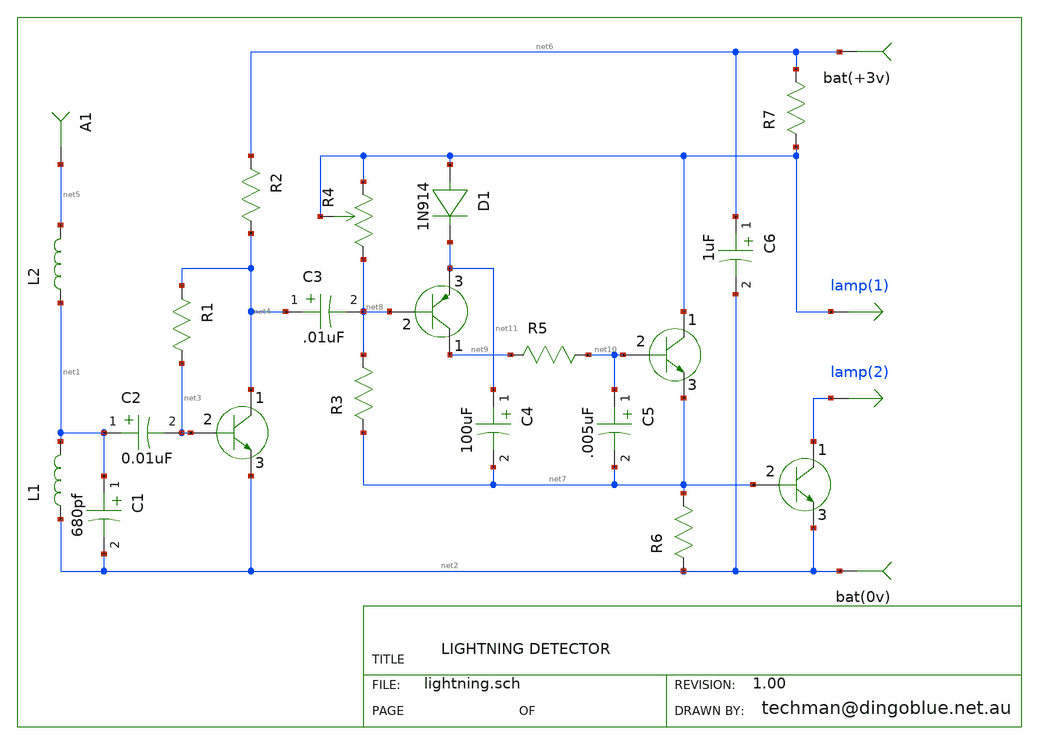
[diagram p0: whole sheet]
** sch_path: xschem_library/gschem_import/lightning.sch
**.subckt lightning
L1 net1 net2 10mH
L2 net5 net1 10mH
C2 net1 net3 0.01uF
C1 net1 net2 680pf
C3 net4 net8 .01uF
C4 net11 net7 100uF
C5 net10 net7 .005uF
R1 net3 net4 180k
R2 net4 net6 3.9k
R7 net6 xxx 47R
R3 net8 net7 22k
R5 net10 net9 2.2K
R6 net7 net2 2.7k
R4 xxx xxx net8 20k
bat(+3v) net6
bat(0v) net2
A1 net5
C6 net6 net2 1uF
D1 xxx net11 1N914
Q1 net4 net2 net3 2N4401
Q2 net9 net11 net8 2N4403
Q3 xxx net7 net10 2N4401
Q4 xxx net2 net7 2N4401
**.ends
.end
